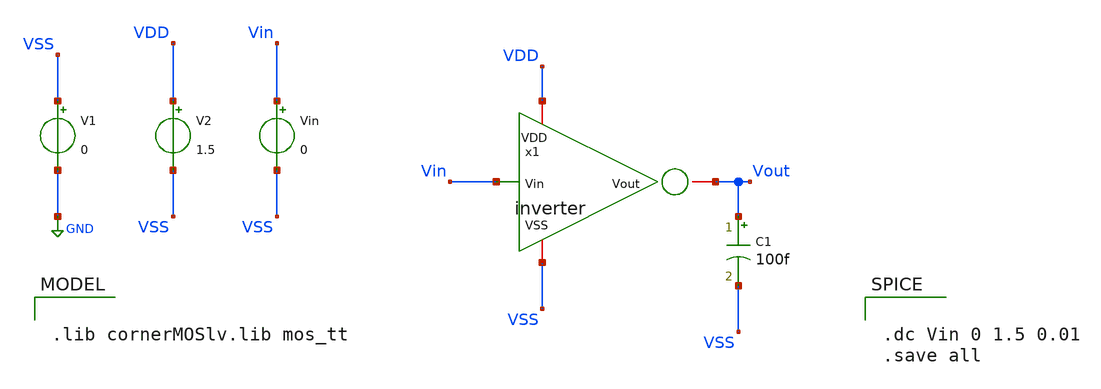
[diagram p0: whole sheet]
** sch_path: Modulo_Analogico/Lab2/inverter_tb.sch
**.subckt inverter_tb
C1 Vout VSS 100f m=1
V1 VSS GND 0
V2 VDD VSS 1.5
Vin Vin VSS 0
x1 Vin VDD VSS Vout inverter
**** begin user architecture code


.dc Vin 0 1.5 0.01
.save all



.lib cornerMOSlv.lib mos_tt

**** end user architecture code
**.ends
.GLOBAL GND
.end
